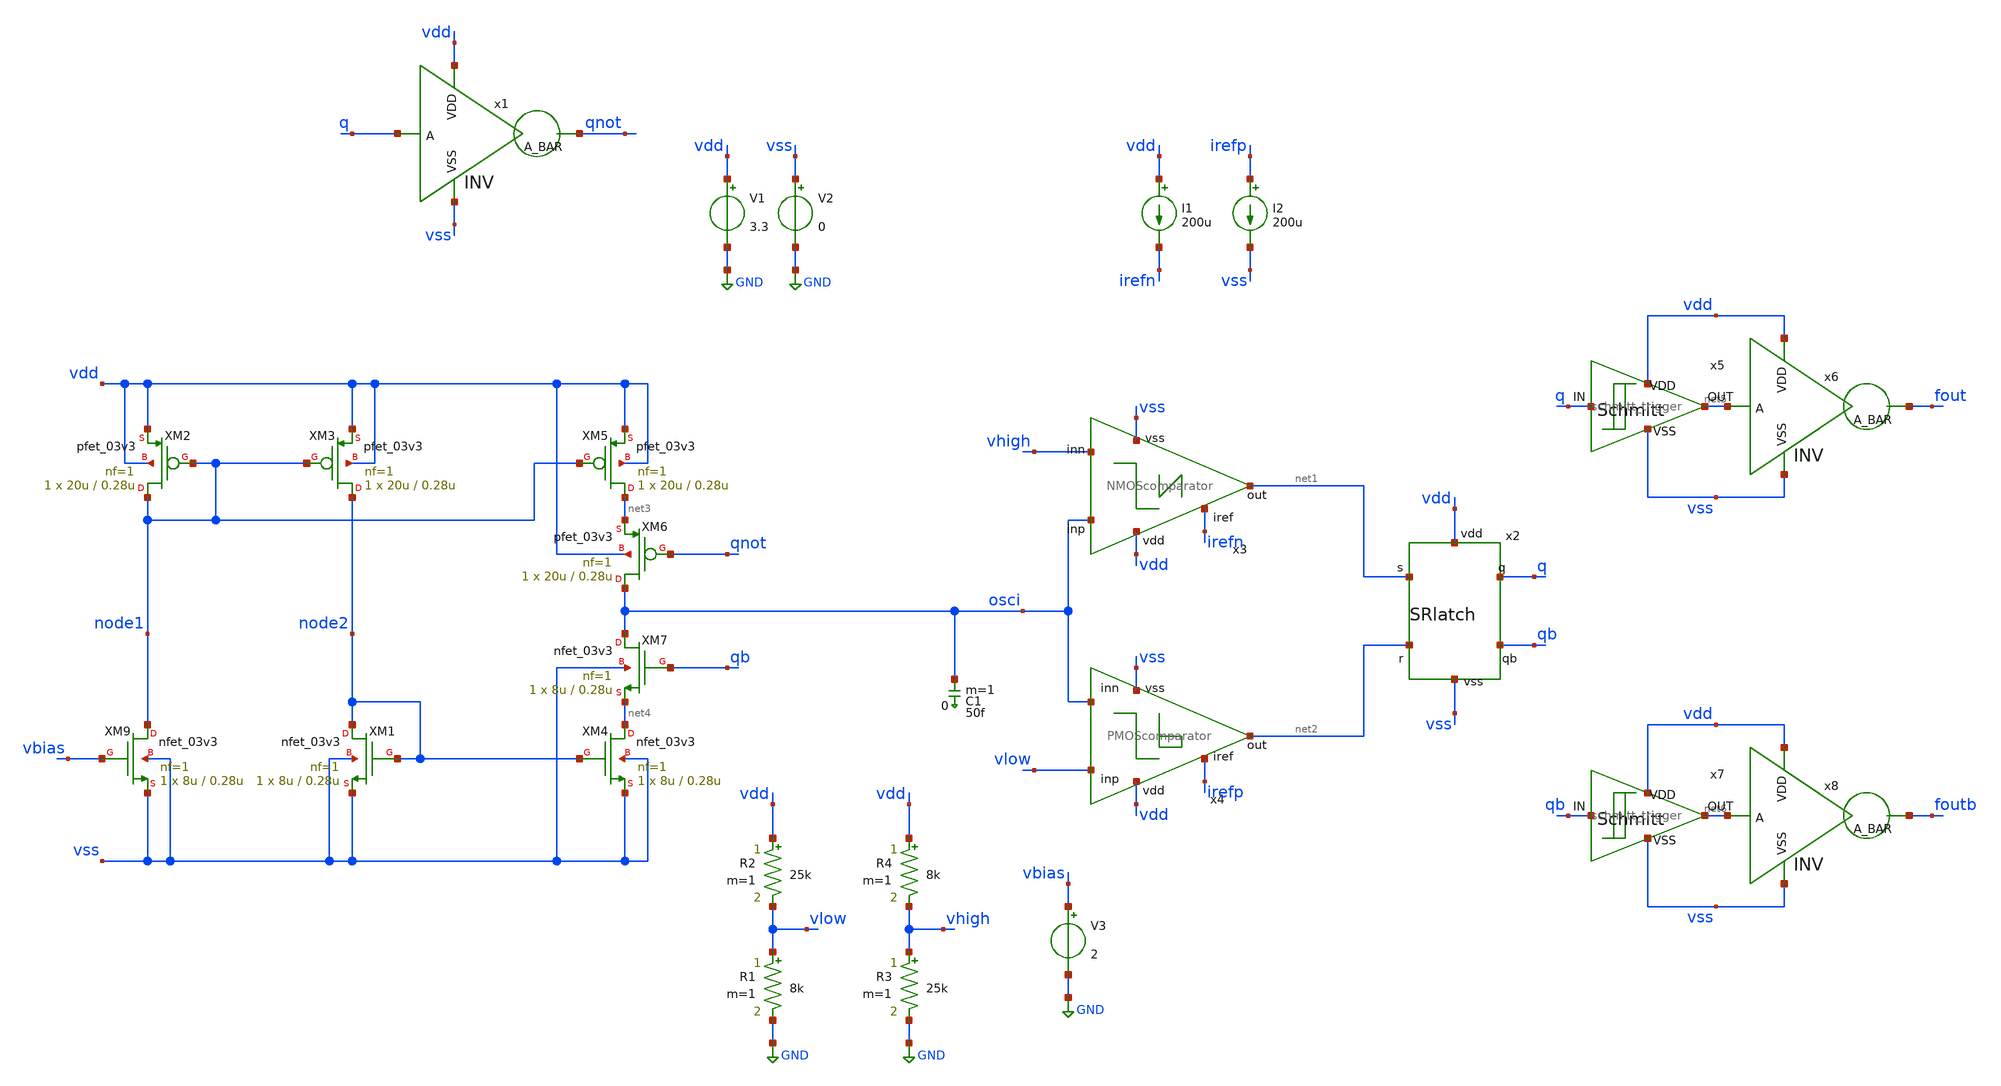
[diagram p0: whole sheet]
** sch_path: designs/libs/qw_core_analog/RVCO/VCROwithCP.sch
**.subckt VCROwithCP
x2 vdd net1 q qb net2 vss SRlatch
V1 vdd GND 3.3
V2 vss GND 0
C1 osci 0 50f m=1
x3 vdd osci net1 vhigh irefn vss NMOScomparator
x4 vdd irefp vlow net2 osci vss PMOScomparator
I1 vdd irefn 200u
I2 irefp vss 200u
XM1 node2 node2 vss vss nfet_03v3 L=0.28u W=8u nf=1 ad='int((nf+1)/2) * W/nf * 0.18u' as='int((nf+2)/2) * W/nf * 0.18u'
+ pd='2*int((nf+1)/2) * (W/nf + 0.18u)' ps='2*int((nf+2)/2) * (W/nf + 0.18u)' nrd='0.18u / W' nrs='0.18u / W'
+ sa=0 sb=0 sd=0 m=1
XM2 node1 node1 vdd vdd pfet_03v3 L=0.28u W=20u nf=1 ad='int((nf+1)/2) * W/nf * 0.18u' as='int((nf+2)/2) * W/nf * 0.18u'
+ pd='2*int((nf+1)/2) * (W/nf + 0.18u)' ps='2*int((nf+2)/2) * (W/nf + 0.18u)' nrd='0.18u / W' nrs='0.18u / W'
+ sa=0 sb=0 sd=0 m=1
XM3 node2 node1 vdd vdd pfet_03v3 L=0.28u W=20u nf=1 ad='int((nf+1)/2) * W/nf * 0.18u' as='int((nf+2)/2) * W/nf * 0.18u'
+ pd='2*int((nf+1)/2) * (W/nf + 0.18u)' ps='2*int((nf+2)/2) * (W/nf + 0.18u)' nrd='0.18u / W' nrs='0.18u / W'
+ sa=0 sb=0 sd=0 m=1
XM4 net4 node2 vss vss nfet_03v3 L=0.28u W=8u nf=1 ad='int((nf+1)/2) * W/nf * 0.18u' as='int((nf+2)/2) * W/nf * 0.18u'
+ pd='2*int((nf+1)/2) * (W/nf + 0.18u)' ps='2*int((nf+2)/2) * (W/nf + 0.18u)' nrd='0.18u / W' nrs='0.18u / W'
+ sa=0 sb=0 sd=0 m=1
XM5 net3 node1 vdd vdd pfet_03v3 L=0.28u W=20u nf=1 ad='int((nf+1)/2) * W/nf * 0.18u' as='int((nf+2)/2) * W/nf * 0.18u'
+ pd='2*int((nf+1)/2) * (W/nf + 0.18u)' ps='2*int((nf+2)/2) * (W/nf + 0.18u)' nrd='0.18u / W' nrs='0.18u / W'
+ sa=0 sb=0 sd=0 m=1
XM6 osci qnot net3 vdd pfet_03v3 L=0.28u W=20u nf=1 ad='int((nf+1)/2) * W/nf * 0.18u' as='int((nf+2)/2) * W/nf * 0.18u'
+ pd='2*int((nf+1)/2) * (W/nf + 0.18u)' ps='2*int((nf+2)/2) * (W/nf + 0.18u)' nrd='0.18u / W' nrs='0.18u / W'
+ sa=0 sb=0 sd=0 m=1
XM7 osci qb net4 vss nfet_03v3 L=0.28u W=8u nf=1 ad='int((nf+1)/2) * W/nf * 0.18u' as='int((nf+2)/2) * W/nf * 0.18u'
+ pd='2*int((nf+1)/2) * (W/nf + 0.18u)' ps='2*int((nf+2)/2) * (W/nf + 0.18u)' nrd='0.18u / W' nrs='0.18u / W'
+ sa=0 sb=0 sd=0 m=1
XM9 node1 vbias vss vss nfet_03v3 L=0.28u W=8u nf=1 ad='int((nf+1)/2) * W/nf * 0.18u' as='int((nf+2)/2) * W/nf * 0.18u'
+ pd='2*int((nf+1)/2) * (W/nf + 0.18u)' ps='2*int((nf+2)/2) * (W/nf + 0.18u)' nrd='0.18u / W' nrs='0.18u / W'
+ sa=0 sb=0 sd=0 m=1
x1 vdd q qnot vss INV
V3 vbias GND 2
R1 vlow GND 8k m=1
R2 vdd vlow 25k m=1
R3 vhigh GND 25k m=1
R4 vdd vhigh 8k m=1
x5 q net5 vdd vss schmitt_trigger
x6 vdd net5 fout vss INV
x7 qb net6 vdd vss schmitt_trigger
x8 vdd net6 foutb vss INV
**** begin user architecture code

.include $::180MCU_MODELS/design.ngspice
.lib $::180MCU_MODELS/sm141064.ngspice typical



.control
save all

**OP
**show all > op.log
**show all

** Source settings
**alter @V5[PULSE] = [ 1.64 1.66 20n 0.1n 0.1n 19.98n 40n 0 ]
**alter @V4[PULSE] = [ 1.66 1.64 20n 0.1n 0.1n 19.98n 40n 0 ]
**alter @V3[PULSE] = [ 0 3.3 10n 0.01n 0.01n 9.98n 20n 0 ]
**alter @V4[PULSE] = [ 0 3.3 50u 0.1u 0.1u 49.8u 100u 0 ]
alter @V1[PULSE] = [ 0 3.3 5n 1n 1n 49.998u 100u 0 ]

** Simulation settings

tran 1p 20n UIC

write VCROwithCP.raw
.endc


**** end user architecture code
**.ends
.GLOBAL GND
.end
